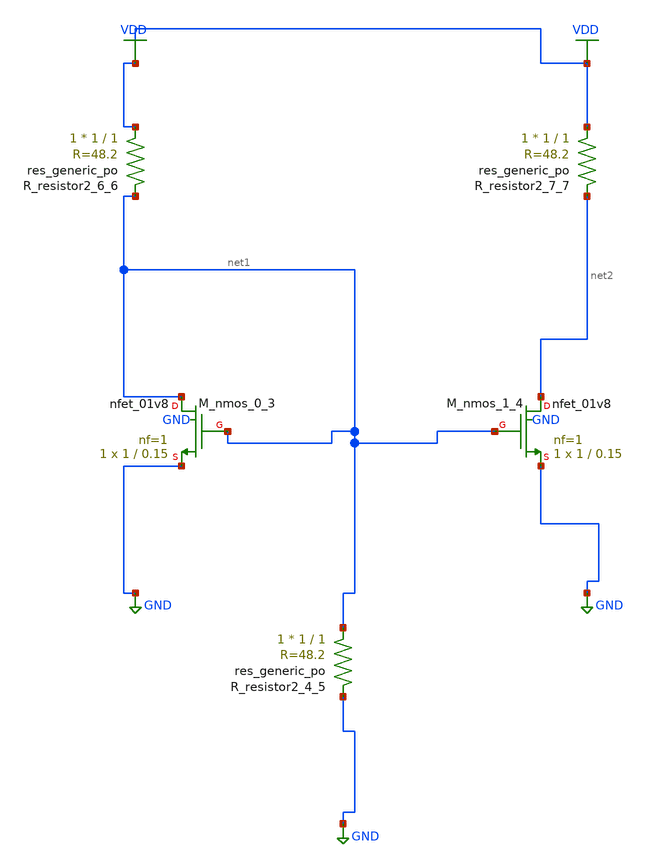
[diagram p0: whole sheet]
** sch_path: schematics/AMSNet/323.sch
**.subckt 323
XM_nmos_0_3 net1 net1 GND GND sky130_fd_pr__nfet_01v8 L=0.15 W=1 nf=1 ad='int((1 + 1)/2) * 1 / 1 * 0.29'
+ as='int((1 + 2)/2) * 1 / 1 * 0.29' pd='2*int((1 + 1)/2) * (1 / 1 + 0.29)' ps='2*int((1 + 2)/2) * (1 / 1 + 0.29)'
+ nrd='0.29 / 1 ' nrs='0.29 / 1 ' sa=0 sb=0 sd=0 mult=1 m=1
XM_nmos_1_4 net2 net1 GND GND sky130_fd_pr__nfet_01v8 L=0.15 W=1 nf=1 ad='int((1 + 1)/2) * 1 / 1 * 0.29'
+ as='int((1 + 2)/2) * 1 / 1 * 0.29' pd='2*int((1 + 1)/2) * (1 / 1 + 0.29)' ps='2*int((1 + 2)/2) * (1 / 1 + 0.29)'
+ nrd='0.29 / 1 ' nrs='0.29 / 1 ' sa=0 sb=0 sd=0 mult=1 m=1
XR_resistor2_4_5 net1 GND sky130_fd_pr__res_generic_po W=1 L=1 m=1
XR_resistor2_6_6 VDD net1 sky130_fd_pr__res_generic_po W=1 L=1 m=1
XR_resistor2_7_7 VDD net2 sky130_fd_pr__res_generic_po W=1 L=1 m=1
**.ends
.GLOBAL GND
.GLOBAL VDD
.end
